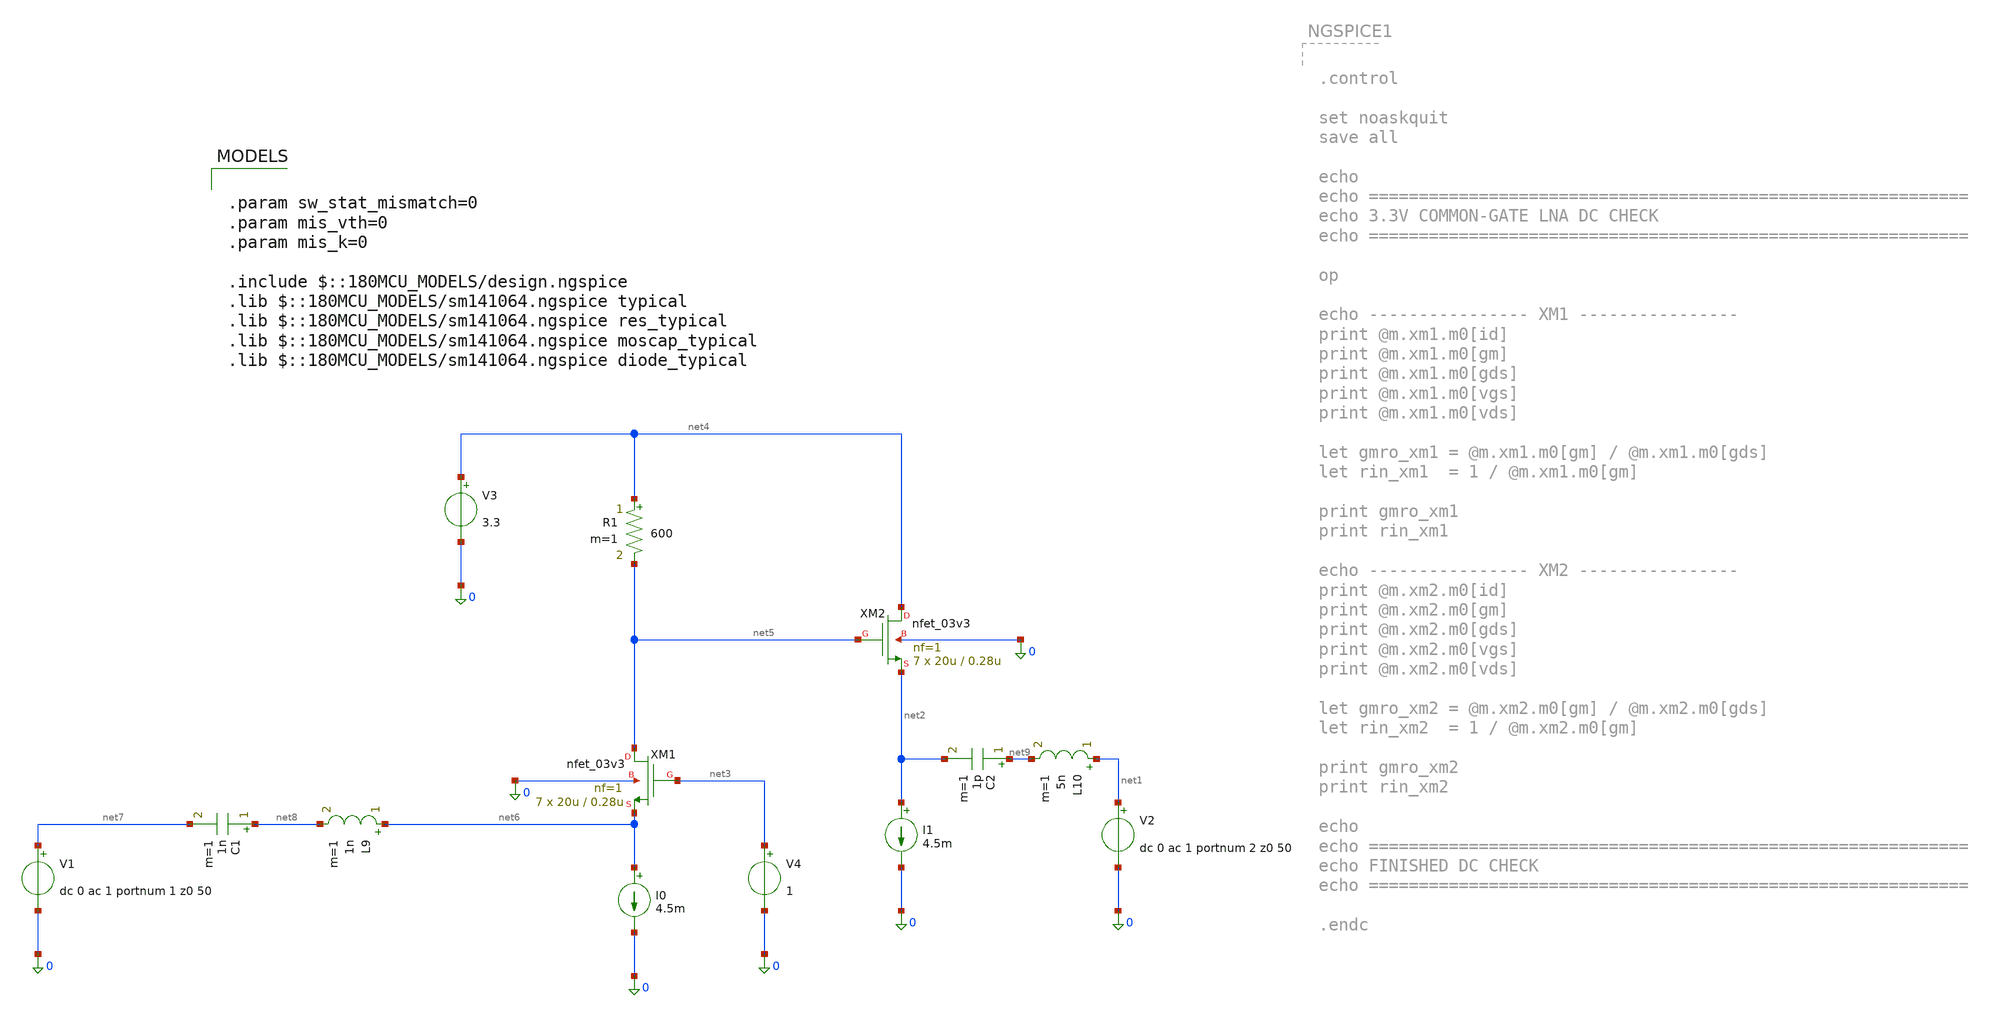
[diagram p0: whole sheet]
** sch_path: LNA_gain_test/test_3p3v.sch
**.subckt test_3p3v
I0 net6 0 4.5m
XM1 net5 net3 net6 0 nfet_03v3 L=0.28u W=20u nf=1 ad='int((nf+1)/2) * W/nf * 0.18u' as='int((nf+2)/2) * W/nf * 0.18u'
+ pd='2*int((nf+1)/2) * (W/nf + 0.18u)' ps='2*int((nf+2)/2) * (W/nf + 0.18u)' nrd='0.18u / W' nrs='0.18u / W'
+ sa=0 sb=0 sd=0 m=7
C1 net8 net7 1n m=1
C2 net9 net2 1p m=1
XM2 net4 net5 net2 0 nfet_03v3 L=0.28u W=20u nf=1 ad='int((nf+1)/2) * W/nf * 0.18u' as='int((nf+2)/2) * W/nf * 0.18u'
+ pd='2*int((nf+1)/2) * (W/nf + 0.18u)' ps='2*int((nf+2)/2) * (W/nf + 0.18u)' nrd='0.18u / W' nrs='0.18u / W'
+ sa=0 sb=0 sd=0 m=7
I1 net2 0 4.5m
V1 net7 0 dc 0 ac 1 portnum 1 z0 50
V2 net1 0 dc 0 ac 1 portnum 2 z0 50
R1 net4 net5 600 m=1
V3 net4 0 3.3
V4 net3 0 1
L9 net6 net8 1n m=1
L10 net1 net9 5n m=1
**** begin user architecture code

.param sw_stat_mismatch=0
.param mis_vth=0
.param mis_k=0

.include $::180MCU_MODELS/design.ngspice
.lib $::180MCU_MODELS/sm141064.ngspice typical
.lib $::180MCU_MODELS/sm141064.ngspice res_typical
.lib $::180MCU_MODELS/sm141064.ngspice moscap_typical
.lib $::180MCU_MODELS/sm141064.ngspice diode_typical



.control

set noaskquit
set wr_singlescale
set wr_vecnames
save all

echo
echo ============================================================
echo 3.3V CG LNA - 2.4 GHz GAIN DIAGNOSTIC
echo Input match is frozen
echo ============================================================

op

echo
echo ---------------- DC CHECK ----------------
print @m.xm1.m0[id]
print @m.xm1.m0[gm]
print @m.xm1.m0[gds]
print @m.xm1.m0[vgs]
print @m.xm1.m0[vds]

print @m.xm2.m0[id]
print @m.xm2.m0[gm]
print @m.xm2.m0[gds]
print @m.xm2.m0[vgs]
print @m.xm2.m0[vds]

let gmro_xm1 = @m.xm1.m0[gm] / @m.xm1.m0[gds]
let gmro_xm2 = @m.xm2.m0[gm] / @m.xm2.m0[gds]

print gmro_xm1
print gmro_xm2

echo
echo ============================================================
echo RUNNING S-PARAMETER SWEEP
echo ============================================================

sp dec 501 10Meg 10G

let s11_db = db(sp1.s_1_1)
let s21_db = db(sp1.s_2_1)
let s12_db = db(sp1.s_1_2)
let s22_db = db(sp1.s_2_2)

let s11_mag = mag(sp1.s_1_1)
let s21_mag = mag(sp1.s_2_1)
let s22_mag = mag(sp1.s_2_2)

let s11_phase = 180/pi * ph(sp1.s_1_1)
let s21_phase = 180/pi * ph(sp1.s_2_1)
let s22_phase = 180/pi * ph(sp1.s_2_2)

let z0 = 50

let zin = z0 * (1 + sp1.s_1_1) / (1 - sp1.s_1_1)
let zin_re = real(zin)
let zin_im = imag(zin)
let zin_mag = mag(zin)

let zout = z0 * (1 + sp1.s_2_2) / (1 - sp1.s_2_2)
let zout_re = real(zout)
let zout_im = imag(zout)
let zout_mag = mag(zout)

echo
echo ============================================================
echo EXACT RESULTS AT 2.4 GHz
echo ============================================================

meas sp s11_2p4g find s11_db at=2.4G
meas sp s21_2p4g find s21_db at=2.4G
meas sp s12_2p4g find s12_db at=2.4G
meas sp s22_2p4g find s22_db at=2.4G

meas sp s11_mag_2p4g find s11_mag at=2.4G
meas sp s21_mag_2p4g find s21_mag at=2.4G
meas sp s22_mag_2p4g find s22_mag at=2.4G

meas sp zin_re_2p4g find zin_re at=2.4G
meas sp zin_im_2p4g find zin_im at=2.4G
meas sp zin_mag_2p4g find zin_mag at=2.4G

meas sp zout_re_2p4g find zout_re at=2.4G
meas sp zout_im_2p4g find zout_im at=2.4G
meas sp zout_mag_2p4g find zout_mag at=2.4G

echo
echo ============================================================
echo GAIN PEAK SEARCH
echo ============================================================

meas sp s21_peak_100m_6g max s21_db from=100Meg to=6G
meas sp s21_peak_freq_100m_6g when s21_db=s21_peak_100m_6g from=100Meg to=6G

meas sp s21_peak_1g_4g max s21_db from=1G to=4G
meas sp s21_peak_freq_1g_4g when s21_db=s21_peak_1g_4g from=1G to=4G

meas sp s11_min_1g_4g min s11_db from=1G to=4G
meas sp s22_min_1g_4g min s22_db from=1G to=4G

echo
echo ============================================================
echo PLOTS
echo ============================================================

plot s21_db title '3.3V CG LNA - S21 Gain'
plot s11_db s22_db title '3.3V CG LNA - S11 and S22'
plot zin_re zin_im title '3.3V CG LNA - Input Impedance'
plot zout_re zout_im title '3.3V CG LNA - Output Impedance'

echo
echo ============================================================
echo WRITING CSV FILE
echo ============================================================

wrdata lna_3v3_gain_diagnostic.csv frequency s11_db s21_db s12_db s22_db s11_mag s21_mag s22_mag
+ s11_phase s21_phase s22_phase zin_re zin_im zin_mag zout_re zout_im zout_mag

echo
echo ============================================================
echo GAIN DIAGNOSTIC COMPLETE
echo Wrote file:
echo lna_3v3_gain_diagnostic.csv
echo ============================================================

.endc


**** end user architecture code
**.ends
.end
